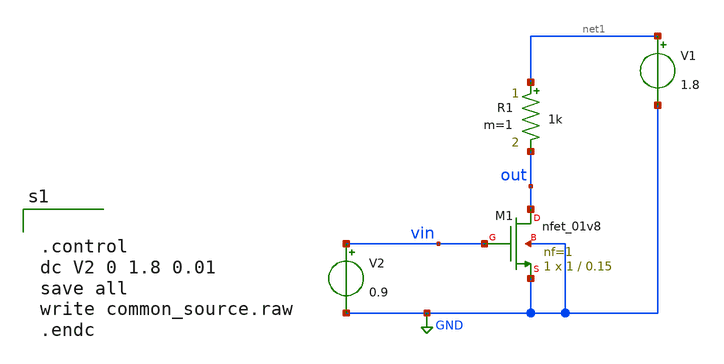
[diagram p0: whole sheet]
** sch_path: xschem/src/common_source/common_source.sch
**.subckt common_source
XM1 out vin GND GND sky130_fd_pr__nfet_01v8 L=0.15 W=1 nf=1 ad='int((nf+1)/2) * W/nf * 0.29' as='int((nf+2)/2) * W/nf * 0.29'
+ pd='2*int((nf+1)/2) * (W/nf + 0.29)' ps='2*int((nf+2)/2) * (W/nf + 0.29)' nrd='0.29 / W' nrs='0.29 / W'
+ sa=0 sb=0 sd=0 mult=1 m=1
V1 net1 GND 1.8
V2 vin GND 0.9
R1 net1 out 1k m=1
**** begin user architecture code

.include $::SKYWATER_MODELS/cells/nfet_01v8/sky130_fd_pr__nfet_01v8__tt.corner.spice
.include $::SKYWATER_MODELS/cells/nfet_01v8_lvt/sky130_fd_pr__nfet_01v8_lvt__tt.corner.spice
.include $::SKYWATER_MODELS/cells/pfet_01v8/sky130_fd_pr__pfet_01v8__tt.corner.spice
.include $::SKYWATER_MODELS/cells/nfet_03v3_nvt/sky130_fd_pr__nfet_03v3_nvt__tt.corner.spice
.include $::SKYWATER_MODELS/cells/nfet_05v0_nvt/sky130_fd_pr__nfet_05v0_nvt__tt.corner.spice
.include $::SKYWATER_MODELS/cells/esd_nfet_01v8/sky130_fd_pr__esd_nfet_01v8__tt.corner.spice
.include $::SKYWATER_MODELS/cells/pfet_01v8_lvt/sky130_fd_pr__pfet_01v8_lvt__tt.corner.spice
.include $::SKYWATER_MODELS/cells/pfet_01v8_hvt/sky130_fd_pr__pfet_01v8_hvt__tt.corner.spice
.include $::SKYWATER_MODELS/cells/esd_pfet_g5v0d10v5/sky130_fd_pr__esd_pfet_g5v0d10v5__tt.corner.spice
.include $::SKYWATER_MODELS/cells/pfet_g5v0d10v5/sky130_fd_pr__pfet_g5v0d10v5__tt.corner.spice
.include $::SKYWATER_MODELS/cells/pfet_g5v0d16v0/sky130_fd_pr__pfet_g5v0d16v0__tt.corner.spice
.include $::SKYWATER_MODELS/cells/nfet_g5v0d10v5/sky130_fd_pr__nfet_g5v0d10v5__tt.corner.spice
.include $::SKYWATER_MODELS/cells/nfet_g5v0d16v0/sky130_fd_pr__nfet_g5v0d16v0__tt_discrete.corner.spice
.include $::SKYWATER_MODELS/cells/esd_nfet_g5v0d10v5/sky130_fd_pr__esd_nfet_g5v0d10v5__tt.corner.spice
.include $::SKYWATER_MODELS/models/corners/tt/nonfet.spice
* Mismatch parameters
.include $::SKYWATER_MODELS/cells/nfet_01v8/sky130_fd_pr__nfet_01v8__mismatch.corner.spice
.include $::SKYWATER_MODELS/cells/pfet_01v8/sky130_fd_pr__pfet_01v8__mismatch.corner.spice
.include $::SKYWATER_MODELS/cells/nfet_01v8_lvt/sky130_fd_pr__nfet_01v8_lvt__mismatch.corner.spice
.include $::SKYWATER_MODELS/cells/pfet_01v8_lvt/sky130_fd_pr__pfet_01v8_lvt__mismatch.corner.spice
.include $::SKYWATER_MODELS/cells/pfet_01v8_hvt/sky130_fd_pr__pfet_01v8_hvt__mismatch.corner.spice
.include $::SKYWATER_MODELS/cells/nfet_g5v0d10v5/sky130_fd_pr__nfet_g5v0d10v5__mismatch.corner.spice
.include $::SKYWATER_MODELS/cells/pfet_g5v0d10v5/sky130_fd_pr__pfet_g5v0d10v5__mismatch.corner.spice
.include $::SKYWATER_MODELS/cells/nfet_05v0_nvt/sky130_fd_pr__nfet_05v0_nvt__mismatch.corner.spice
.include $::SKYWATER_MODELS/cells/nfet_03v3_nvt/sky130_fd_pr__nfet_03v3_nvt__mismatch.corner.spice
* Resistor$::SKYWATER_MODELS/Capacitor
.include $::SKYWATER_MODELS/models/r+c/res_typical__cap_typical.spice
.include $::SKYWATER_MODELS/models/r+c/res_typical__cap_typical__lin.spice
* Special cells
.include $::SKYWATER_MODELS/models/corners/tt/specialized_cells.spice
* All models
.include $::SKYWATER_MODELS/models/all.spice
* Corner
.include $::SKYWATER_MODELS/models/corners/tt/rf.spice



.control
dc V2 0 1.8 0.01
save all
write common_source.raw
.endc


**** end user architecture code
**.ends
.GLOBAL GND
.end
